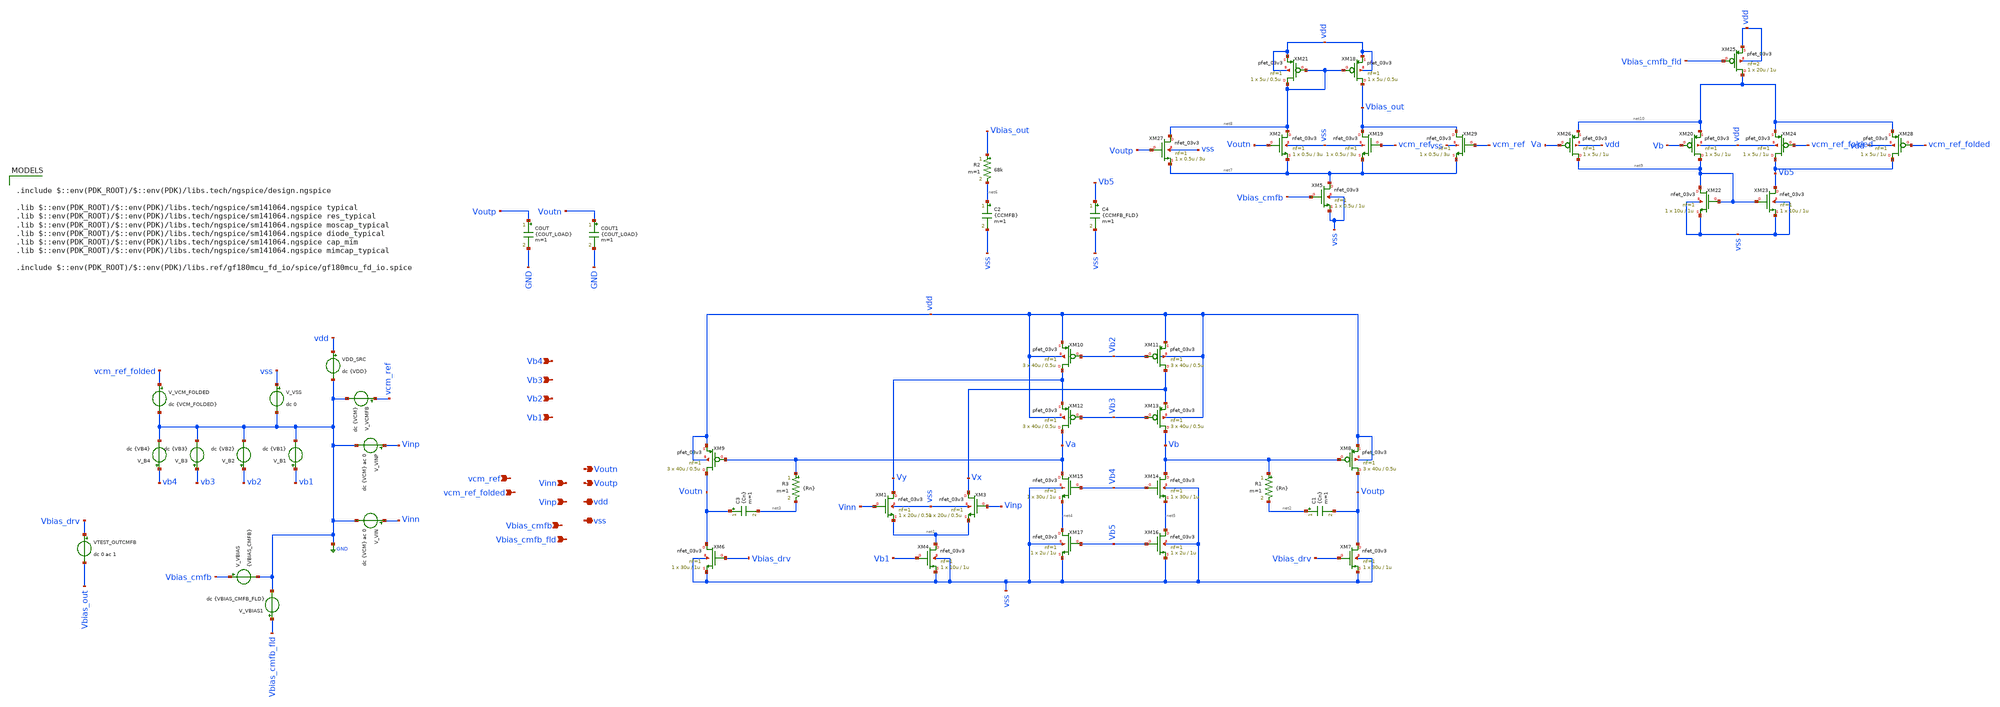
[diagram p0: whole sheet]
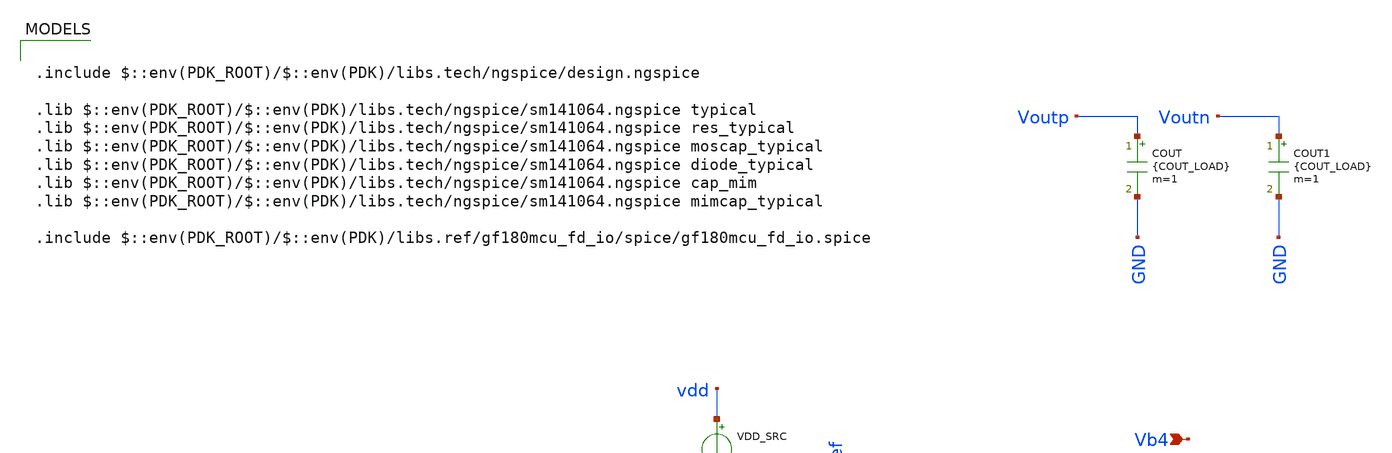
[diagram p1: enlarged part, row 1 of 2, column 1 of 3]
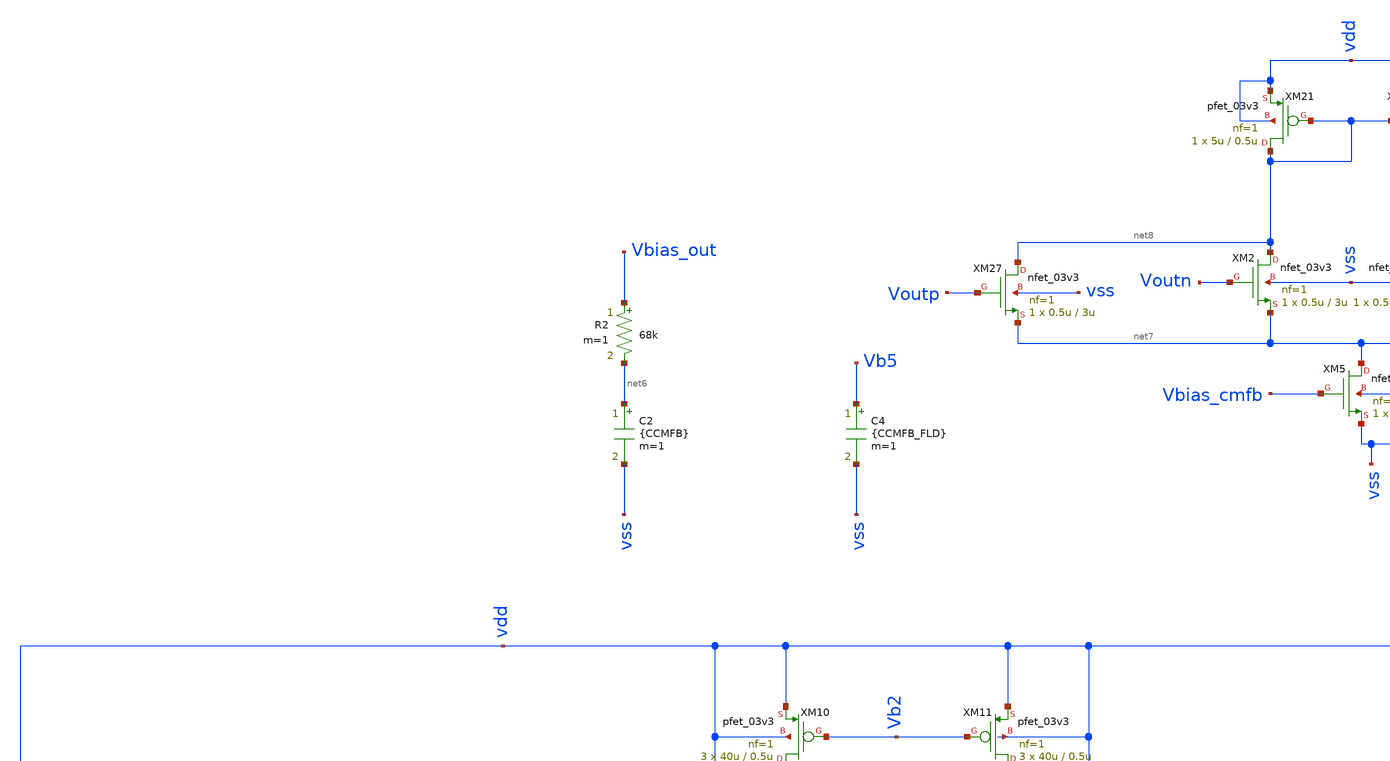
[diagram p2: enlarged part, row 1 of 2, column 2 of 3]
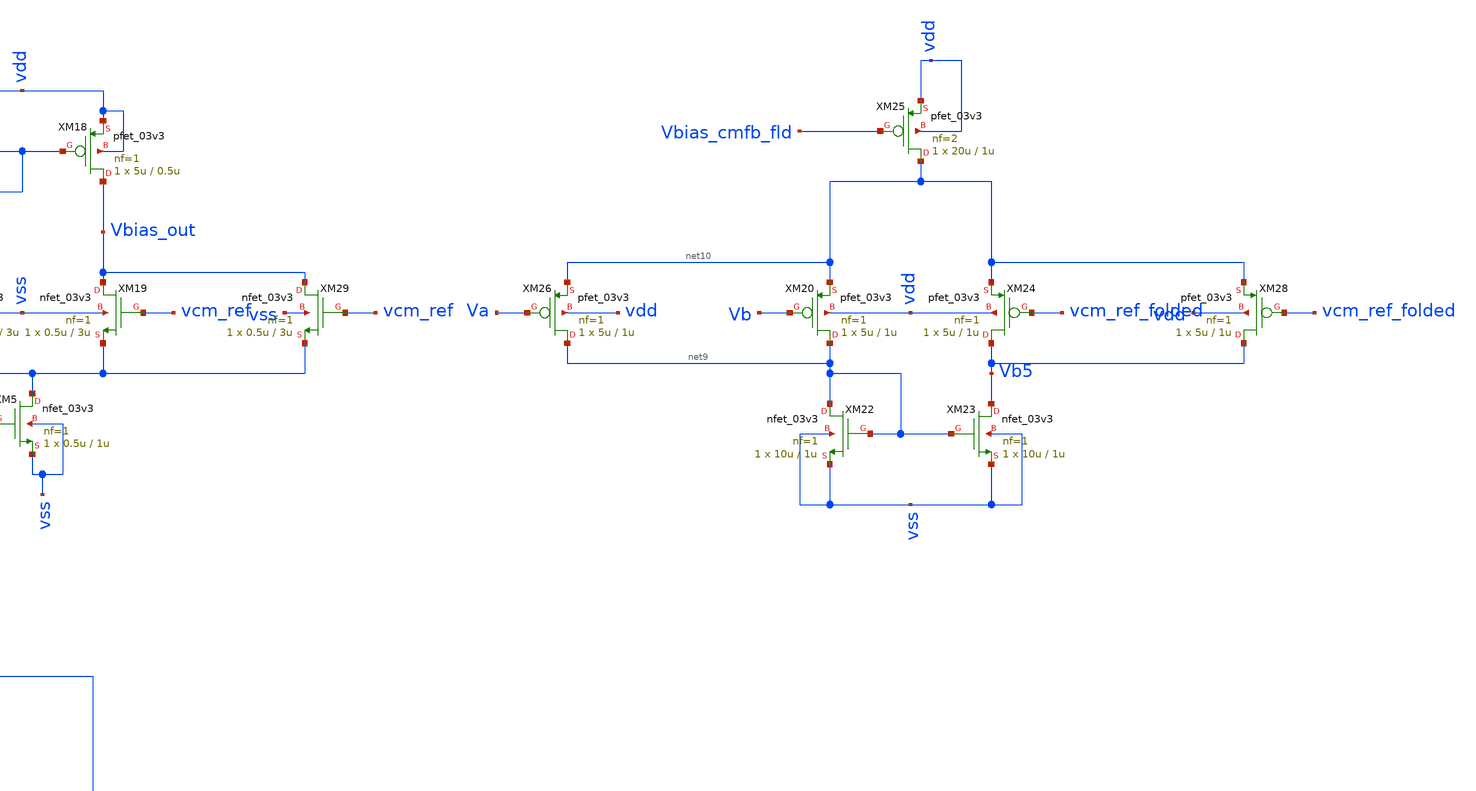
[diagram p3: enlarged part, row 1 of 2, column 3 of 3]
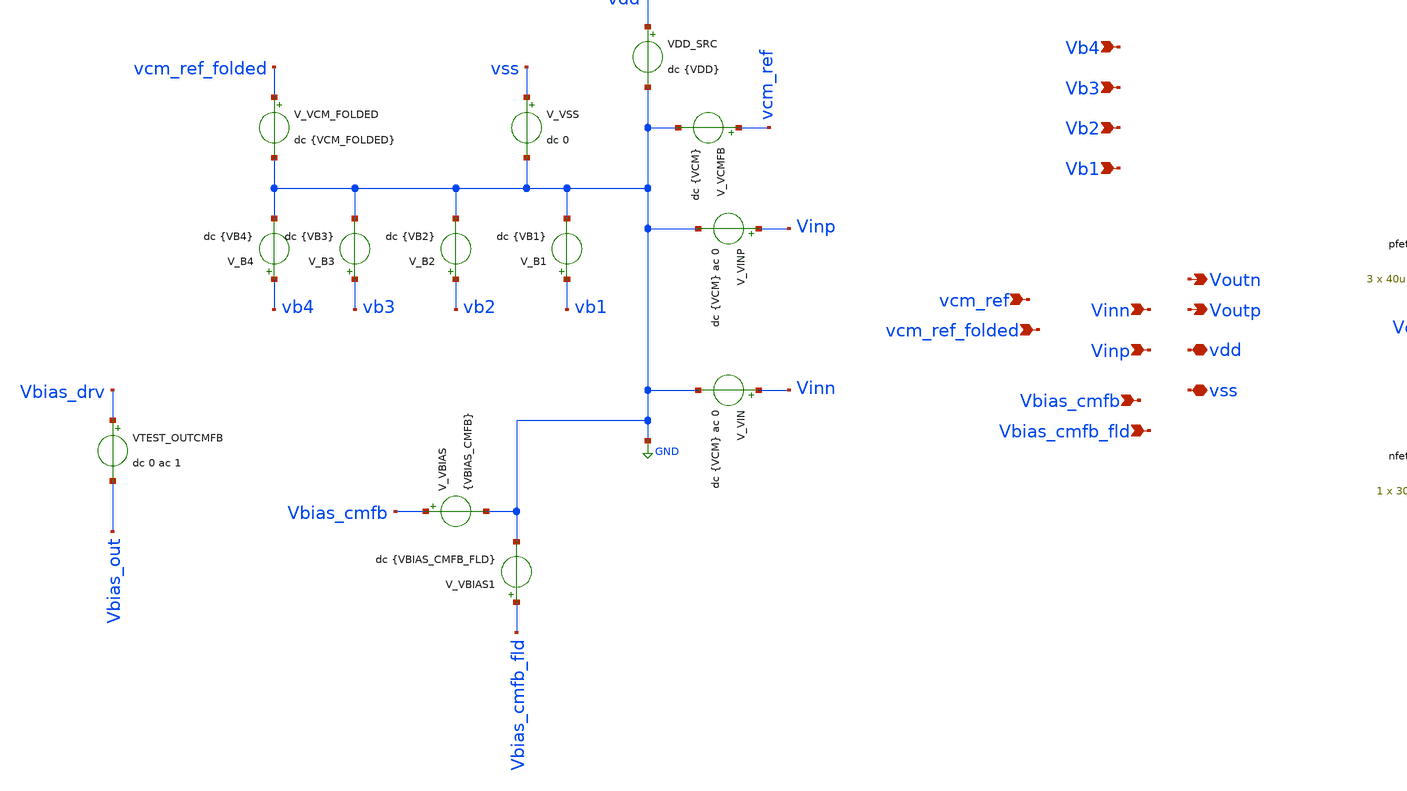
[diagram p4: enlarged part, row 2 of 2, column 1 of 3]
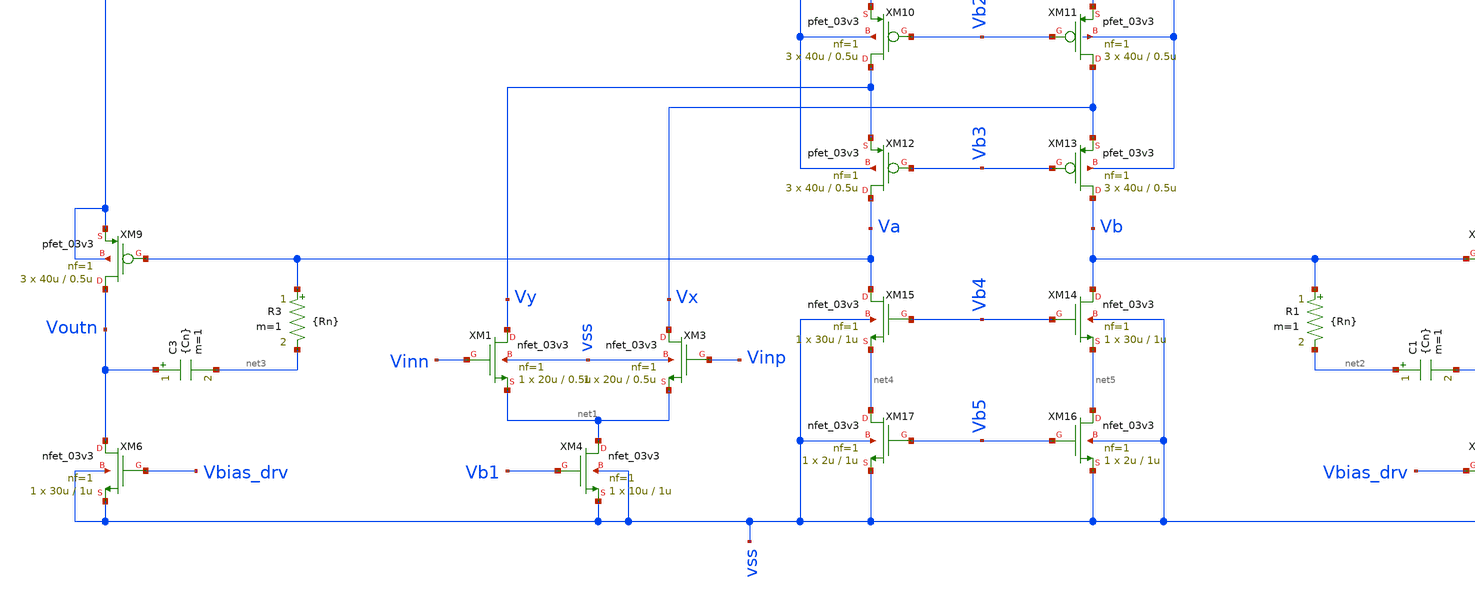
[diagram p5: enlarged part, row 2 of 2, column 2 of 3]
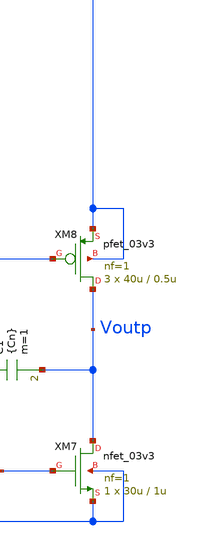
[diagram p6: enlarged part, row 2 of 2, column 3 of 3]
** sch_path: circuit_files/tb/op-amp_diff_looptest.sch
**.subckt op-amp_diff_looptest Vinn Voutp vdd Vinp Vb1 Vbias_cmfb_fld vss Voutn Vbias_cmfb Vb2 Vb3
*+ Vb4 vcm_ref_folded vcm_ref
*.ipin Vinn
*.opin Voutp
*.iopin vdd
*.ipin Vinp
*.ipin Vb1
*.ipin Vbias_cmfb_fld
*.iopin vss
*.opin Voutn
*.ipin Vbias_cmfb
*.ipin Vb2
*.ipin Vb3
*.ipin Vb4
*.ipin vcm_ref_folded
*.ipin vcm_ref
XM1 Vy Vinn net1 vss nfet_03v3 L=0.5u W=20u nf=1 ad='int((nf+1)/2) * W/nf * 0.18u' as='int((nf+2)/2) * W/nf * 0.18u'
+ pd='2*int((nf+1)/2) * (W/nf + 0.18u)' ps='2*int((nf+2)/2) * (W/nf + 0.18u)' nrd='0.18u / W' nrs='0.18u / W'
+ sa=0 sb=0 sd=0 m=1
XM4 net1 Vb1 vss vss nfet_03v3 L=1u W=10u nf=1 ad='int((nf+1)/2) * W/nf * 0.18u' as='int((nf+2)/2) * W/nf * 0.18u'
+ pd='2*int((nf+1)/2) * (W/nf + 0.18u)' ps='2*int((nf+2)/2) * (W/nf + 0.18u)' nrd='0.18u / W' nrs='0.18u / W'
+ sa=0 sb=0 sd=0 m=1
XM3 Vx Vinp net1 vss nfet_03v3 L=0.5u W=20u nf=1 ad='int((nf+1)/2) * W/nf * 0.18u' as='int((nf+2)/2) * W/nf * 0.18u'
+ pd='2*int((nf+1)/2) * (W/nf + 0.18u)' ps='2*int((nf+2)/2) * (W/nf + 0.18u)' nrd='0.18u / W' nrs='0.18u / W'
+ sa=0 sb=0 sd=0 m=1
XM7 Voutp Vbias_drv vss vss nfet_03v3 L=1u W=30u nf=1 ad='int((nf+1)/2) * W/nf * 0.18u' as='int((nf+2)/2) * W/nf * 0.18u'
+ pd='2*int((nf+1)/2) * (W/nf + 0.18u)' ps='2*int((nf+2)/2) * (W/nf + 0.18u)' nrd='0.18u / W' nrs='0.18u / W'
+ sa=0 sb=0 sd=0 m=1
XM8 Voutp Vb vdd vdd pfet_03v3 L=0.5u W=40u nf=1 ad='int((nf+1)/2) * W/nf * 0.18u' as='int((nf+2)/2) * W/nf * 0.18u'
+ pd='2*int((nf+1)/2) * (W/nf + 0.18u)' ps='2*int((nf+2)/2) * (W/nf + 0.18u)' nrd='0.18u / W' nrs='0.18u / W'
+ sa=0 sb=0 sd=0 m=3
XM6 Voutn Vbias_drv vss vss nfet_03v3 L=1u W=30u nf=1 ad='int((nf+1)/2) * W/nf * 0.18u' as='int((nf+2)/2) * W/nf * 0.18u'
+ pd='2*int((nf+1)/2) * (W/nf + 0.18u)' ps='2*int((nf+2)/2) * (W/nf + 0.18u)' nrd='0.18u / W' nrs='0.18u / W'
+ sa=0 sb=0 sd=0 m=1
XM9 Voutn Va vdd vdd pfet_03v3 L=0.5u W=40u nf=1 ad='int((nf+1)/2) * W/nf * 0.18u' as='int((nf+2)/2) * W/nf * 0.18u'
+ pd='2*int((nf+1)/2) * (W/nf + 0.18u)' ps='2*int((nf+2)/2) * (W/nf + 0.18u)' nrd='0.18u / W' nrs='0.18u / W'
+ sa=0 sb=0 sd=0 m=3
XM10 Vy Vb2 vdd vdd pfet_03v3 L=0.5u W=40u nf=1 ad='int((nf+1)/2) * W/nf * 0.18u' as='int((nf+2)/2) * W/nf * 0.18u'
+ pd='2*int((nf+1)/2) * (W/nf + 0.18u)' ps='2*int((nf+2)/2) * (W/nf + 0.18u)' nrd='0.18u / W' nrs='0.18u / W'
+ sa=0 sb=0 sd=0 m=3
XM11 Vx Vb2 vdd vdd pfet_03v3 L=0.5u W=40u nf=1 ad='int((nf+1)/2) * W/nf * 0.18u' as='int((nf+2)/2) * W/nf * 0.18u'
+ pd='2*int((nf+1)/2) * (W/nf + 0.18u)' ps='2*int((nf+2)/2) * (W/nf + 0.18u)' nrd='0.18u / W' nrs='0.18u / W'
+ sa=0 sb=0 sd=0 m=3
XM12 Va Vb3 Vy vdd pfet_03v3 L=0.5u W=40u nf=1 ad='int((nf+1)/2) * W/nf * 0.18u' as='int((nf+2)/2) * W/nf * 0.18u'
+ pd='2*int((nf+1)/2) * (W/nf + 0.18u)' ps='2*int((nf+2)/2) * (W/nf + 0.18u)' nrd='0.18u / W' nrs='0.18u / W'
+ sa=0 sb=0 sd=0 m=3
XM13 Vb Vb3 Vx vdd pfet_03v3 L=0.5u W=40u nf=1 ad='int((nf+1)/2) * W/nf * 0.18u' as='int((nf+2)/2) * W/nf * 0.18u'
+ pd='2*int((nf+1)/2) * (W/nf + 0.18u)' ps='2*int((nf+2)/2) * (W/nf + 0.18u)' nrd='0.18u / W' nrs='0.18u / W'
+ sa=0 sb=0 sd=0 m=3
XM14 Vb Vb4 net5 vss nfet_03v3 L=1u W=30u nf=1 ad='int((nf+1)/2) * W/nf * 0.18u' as='int((nf+2)/2) * W/nf * 0.18u'
+ pd='2*int((nf+1)/2) * (W/nf + 0.18u)' ps='2*int((nf+2)/2) * (W/nf + 0.18u)' nrd='0.18u / W' nrs='0.18u / W'
+ sa=0 sb=0 sd=0 m=1
XM15 Va Vb4 net4 vss nfet_03v3 L=1u W=30u nf=1 ad='int((nf+1)/2) * W/nf * 0.18u' as='int((nf+2)/2) * W/nf * 0.18u'
+ pd='2*int((nf+1)/2) * (W/nf + 0.18u)' ps='2*int((nf+2)/2) * (W/nf + 0.18u)' nrd='0.18u / W' nrs='0.18u / W'
+ sa=0 sb=0 sd=0 m=1
XM16 net5 Vb5 vss vss nfet_03v3 L=1u W=2u nf=1 ad='int((nf+1)/2) * W/nf * 0.18u' as='int((nf+2)/2) * W/nf * 0.18u'
+ pd='2*int((nf+1)/2) * (W/nf + 0.18u)' ps='2*int((nf+2)/2) * (W/nf + 0.18u)' nrd='0.18u / W' nrs='0.18u / W'
+ sa=0 sb=0 sd=0 m=1
XM17 net4 Vb5 vss vss nfet_03v3 L=1u W=2u nf=1 ad='int((nf+1)/2) * W/nf * 0.18u' as='int((nf+2)/2) * W/nf * 0.18u'
+ pd='2*int((nf+1)/2) * (W/nf + 0.18u)' ps='2*int((nf+2)/2) * (W/nf + 0.18u)' nrd='0.18u / W' nrs='0.18u / W'
+ sa=0 sb=0 sd=0 m=1
C3 Voutn net3 {Cn} m=1
R3 Va net3 {Rn} m=1
R1 Vb net2 {Rn} m=1
C1 net2 Voutp {Cn} m=1
C2 net6 vss {CCMFB} m=1
C4 Vb5 vss {CCMFB_FLD} m=1
V_VIN Vinn GND dc {VCM} ac 0
VDD_SRC vdd GND dc {VDD}
V_VINP Vinp GND dc {VCM} ac 0
V_VSS vss GND dc 0
V_VCMFB vcm_ref GND dc {VCM}
V_B1 vb1 GND dc {VB1}
V_B2 vb2 GND dc {VB2}
V_B3 vb3 GND dc {VB3}
V_B4 vb4 GND dc {VB4}
V_VCM_FOLDED vcm_ref_folded GND dc {VCM_FOLDED}
V_VBIAS Vbias_cmfb GND {VBIAS_CMFB}
V_VBIAS1 Vbias_cmfb_fld GND dc {VBIAS_CMFB_FLD}
COUT Voutp GND {COUT_LOAD} m=1
COUT1 Voutn GND {COUT_LOAD} m=1
VTEST_OUTCMFB Vbias_drv Vbias_out dc 0 ac 1
XM2 net8 Voutn net7 vss nfet_03v3 L=3u W=0.5u nf=1 ad='int((nf+1)/2) * W/nf * 0.18u' as='int((nf+2)/2) * W/nf * 0.18u'
+ pd='2*int((nf+1)/2) * (W/nf + 0.18u)' ps='2*int((nf+2)/2) * (W/nf + 0.18u)' nrd='0.18u / W' nrs='0.18u / W'
+ sa=0 sb=0 sd=0 m=1
XM5 net7 Vbias_cmfb vss vss nfet_03v3 L=1u W=0.5u nf=1 ad='int((nf+1)/2) * W/nf * 0.18u' as='int((nf+2)/2) * W/nf * 0.18u'
+ pd='2*int((nf+1)/2) * (W/nf + 0.18u)' ps='2*int((nf+2)/2) * (W/nf + 0.18u)' nrd='0.18u / W' nrs='0.18u / W'
+ sa=0 sb=0 sd=0 m=1
XM18 Vbias_out net8 vdd vdd pfet_03v3 L=0.5u W=5u nf=1 ad='int((nf+1)/2) * W/nf * 0.18u' as='int((nf+2)/2) * W/nf * 0.18u'
+ pd='2*int((nf+1)/2) * (W/nf + 0.18u)' ps='2*int((nf+2)/2) * (W/nf + 0.18u)' nrd='0.18u / W' nrs='0.18u / W'
+ sa=0 sb=0 sd=0 m=1
XM19 Vbias_out vcm_ref net7 vss nfet_03v3 L=3u W=0.5u nf=1 ad='int((nf+1)/2) * W/nf * 0.18u' as='int((nf+2)/2) * W/nf * 0.18u'
+ pd='2*int((nf+1)/2) * (W/nf + 0.18u)' ps='2*int((nf+2)/2) * (W/nf + 0.18u)' nrd='0.18u / W' nrs='0.18u / W'
+ sa=0 sb=0 sd=0 m=1
XM21 net8 net8 vdd vdd pfet_03v3 L=0.5u W=5u nf=1 ad='int((nf+1)/2) * W/nf * 0.18u' as='int((nf+2)/2) * W/nf * 0.18u'
+ pd='2*int((nf+1)/2) * (W/nf + 0.18u)' ps='2*int((nf+2)/2) * (W/nf + 0.18u)' nrd='0.18u / W' nrs='0.18u / W'
+ sa=0 sb=0 sd=0 m=1
XM20 net9 Vb net10 vdd pfet_03v3 L=1u W=5u nf=1 ad='int((nf+1)/2) * W/nf * 0.18u' as='int((nf+2)/2) * W/nf * 0.18u'
+ pd='2*int((nf+1)/2) * (W/nf + 0.18u)' ps='2*int((nf+2)/2) * (W/nf + 0.18u)' nrd='0.18u / W' nrs='0.18u / W'
+ sa=0 sb=0 sd=0 m=1
XM24 Vb5 vcm_ref_folded net10 vdd pfet_03v3 L=1u W=5u nf=1 ad='int((nf+1)/2) * W/nf * 0.18u' as='int((nf+2)/2) * W/nf * 0.18u'
+ pd='2*int((nf+1)/2) * (W/nf + 0.18u)' ps='2*int((nf+2)/2) * (W/nf + 0.18u)' nrd='0.18u / W' nrs='0.18u / W'
+ sa=0 sb=0 sd=0 m=1
XM22 net9 net9 vss vss nfet_03v3 L=1u W=10u nf=1 ad='int((nf+1)/2) * W/nf * 0.18u' as='int((nf+2)/2) * W/nf * 0.18u'
+ pd='2*int((nf+1)/2) * (W/nf + 0.18u)' ps='2*int((nf+2)/2) * (W/nf + 0.18u)' nrd='0.18u / W' nrs='0.18u / W'
+ sa=0 sb=0 sd=0 m=1
XM23 Vb5 net9 vss vss nfet_03v3 L=1u W=10u nf=1 ad='int((nf+1)/2) * W/nf * 0.18u' as='int((nf+2)/2) * W/nf * 0.18u'
+ pd='2*int((nf+1)/2) * (W/nf + 0.18u)' ps='2*int((nf+2)/2) * (W/nf + 0.18u)' nrd='0.18u / W' nrs='0.18u / W'
+ sa=0 sb=0 sd=0 m=1
XM25 net10 Vbias_cmfb_fld vdd vdd pfet_03v3 L=1u W=20u nf=2 ad='int((nf+1)/2) * W/nf * 0.18u' as='int((nf+2)/2) * W/nf * 0.18u'
+ pd='2*int((nf+1)/2) * (W/nf + 0.18u)' ps='2*int((nf+2)/2) * (W/nf + 0.18u)' nrd='0.18u / W' nrs='0.18u / W'
+ sa=0 sb=0 sd=0 m=1
XM26 net9 Va net10 vdd pfet_03v3 L=1u W=5u nf=1 ad='int((nf+1)/2) * W/nf * 0.18u' as='int((nf+2)/2) * W/nf * 0.18u'
+ pd='2*int((nf+1)/2) * (W/nf + 0.18u)' ps='2*int((nf+2)/2) * (W/nf + 0.18u)' nrd='0.18u / W' nrs='0.18u / W'
+ sa=0 sb=0 sd=0 m=1
XM28 Vb5 vcm_ref_folded net10 vdd pfet_03v3 L=1u W=5u nf=1 ad='int((nf+1)/2) * W/nf * 0.18u' as='int((nf+2)/2) * W/nf * 0.18u'
+ pd='2*int((nf+1)/2) * (W/nf + 0.18u)' ps='2*int((nf+2)/2) * (W/nf + 0.18u)' nrd='0.18u / W' nrs='0.18u / W'
+ sa=0 sb=0 sd=0 m=1
XM27 net8 Voutp net7 vss nfet_03v3 L=3u W=0.5u nf=1 ad='int((nf+1)/2) * W/nf * 0.18u' as='int((nf+2)/2) * W/nf * 0.18u'
+ pd='2*int((nf+1)/2) * (W/nf + 0.18u)' ps='2*int((nf+2)/2) * (W/nf + 0.18u)' nrd='0.18u / W' nrs='0.18u / W'
+ sa=0 sb=0 sd=0 m=1
XM29 Vbias_out vcm_ref net7 vss nfet_03v3 L=3u W=0.5u nf=1 ad='int((nf+1)/2) * W/nf * 0.18u' as='int((nf+2)/2) * W/nf * 0.18u'
+ pd='2*int((nf+1)/2) * (W/nf + 0.18u)' ps='2*int((nf+2)/2) * (W/nf + 0.18u)' nrd='0.18u / W' nrs='0.18u / W'
+ sa=0 sb=0 sd=0 m=1
R2 Vbias_out net6 68k m=1
**** begin user architecture code

.include $::env(PDK_ROOT)/$::env(PDK)/libs.tech/ngspice/design.ngspice

.lib $::env(PDK_ROOT)/$::env(PDK)/libs.tech/ngspice/sm141064.ngspice typical
.lib $::env(PDK_ROOT)/$::env(PDK)/libs.tech/ngspice/sm141064.ngspice res_typical
.lib $::env(PDK_ROOT)/$::env(PDK)/libs.tech/ngspice/sm141064.ngspice moscap_typical
.lib $::env(PDK_ROOT)/$::env(PDK)/libs.tech/ngspice/sm141064.ngspice diode_typical
.lib $::env(PDK_ROOT)/$::env(PDK)/libs.tech/ngspice/sm141064.ngspice cap_mim
.lib $::env(PDK_ROOT)/$::env(PDK)/libs.tech/ngspice/sm141064.ngspice mimcap_typical

.include $::env(PDK_ROOT)/$::env(PDK)/libs.ref/gf180mcu_fd_io/spice/gf180mcu_fd_io.spice



.param VDD=3.3
.param VCM=1.65
.param VCM_FOLDED=2.40

.param VB1=0.58
.param VB2=2.637
.param VB3=2.25
.param VB4=1.15

.param VBIAS_CMFB=0.82
.param VBIAS_CMFB_FLD=2.55

.param Cn=500f
.param Rn=8k
.param COUT_LOAD=200f

.param CCMFB=50p
.param CCMFB_FLD=1p

.options reltol=1e-4 abstol=1e-12 vntol=1e-6
.options gmin=1e-12
.options plotwinsize=0
.options method=gear maxord=2

.nodeset V(voutp)=1.641
.nodeset V(voutn)=1.641
.nodeset V(vbias_out)=0.866
.nodeset V(vbias_drv)=0.866
.nodeset V(va)=2.401
.nodeset V(vb)=2.401
.nodeset V(vb5)=0.716
.nodeset V(net8)=0.576
.nodeset V(net9)=3.194

.control

set noaskquit
set measdgt=8
save all

shell rm -f outcmfb_loop_report.txt
shell rm -f outcmfb_loop_response.txt

echo ================================================== > outcmfb_loop_report.txt
echo OUTPUT CMFB LOOP TEST >> outcmfb_loop_report.txt
echo ================================================== >> outcmfb_loop_report.txt

op

let voutcm_op     = 0.5*(v(voutp)+v(voutn))
let out_cm_err    = voutcm_op-1.65
let va_cm_op      = 0.5*(v(va)+v(vb))
let folded_cm_err = va_cm_op - v(vcm_ref_folded)
let idd_op        = -i(VDD_SRC)
let pdc_op        = 3.3*idd_op

echo ---------------- OP CHECK ---------------- >> outcmfb_loop_report.txt
echo VOUTP=$&v(voutp) >> outcmfb_loop_report.txt
echo VOUTN=$&v(voutn) >> outcmfb_loop_report.txt
echo VOUTCM=$&voutcm_op >> outcmfb_loop_report.txt
echo OUT_CM_ERR=$&out_cm_err >> outcmfb_loop_report.txt

echo VBIAS_OUT=$&v(vbias_out) >> outcmfb_loop_report.txt
echo VBIAS_DRV=$&v(vbias_drv) >> outcmfb_loop_report.txt
echo VA=$&v(va) >> outcmfb_loop_report.txt
echo VB=$&v(vb) >> outcmfb_loop_report.txt
echo VA_CM=$&va_cm_op >> outcmfb_loop_report.txt

echo FOLDED_CM_ERR=$&folded_cm_err >> outcmfb_loop_report.txt
echo IDD=$&idd_op >> outcmfb_loop_report.txt
echo PDC=$&pdc_op >> outcmfb_loop_report.txt
echo -------------------------------------------------- >> outcmfb_loop_report.txt

ac dec 200 1 1G

let outcmfb_inj          = v(vbias_drv)-v(vbias_out)

let outcmfb_return_ratio = -v(vbias_out)/(outcmfb_inj+1e-30)

let outcmfb_loop         = outcmfb_return_ratio/(1-outcmfb_return_ratio+1e-30)
let outcmfb_loop_db      = 20*log10(mag(outcmfb_loop)+1e-30)

let outcmfb_phase_rad    = cph(outcmfb_loop)
let outcmfb_phase_deg    = 57.2957795*outcmfb_phase_rad

meas ac OUTCMFB_GAIN_1HZ_DB  find outcmfb_loop_db at=1
meas ac OUTCMFB_PHASE_1HZ    find outcmfb_phase_deg at=1
meas ac OUTCMFB_UGF          when outcmfb_loop_db=0 fall=1
meas ac OUTCMFB_PHASE_UGF    find outcmfb_phase_deg when outcmfb_loop_db=0 fall=1

let outcmfb_phase_ugf_wrapped = outcmfb_phase_ugf

while outcmfb_phase_ugf_wrapped < -180
  let outcmfb_phase_ugf_wrapped = outcmfb_phase_ugf_wrapped + 360
end

while outcmfb_phase_ugf_wrapped > 180
  let outcmfb_phase_ugf_wrapped = outcmfb_phase_ugf_wrapped - 360
end

let OUTCMFB_PM_RAW = 180 + outcmfb_phase_ugf
let OUTCMFB_PM_WRAPPED = 180 + outcmfb_phase_ugf_wrapped

meas ac OUTCMFB_GAIN_10K     find outcmfb_loop_db at=10k
meas ac OUTCMFB_GAIN_100K    find outcmfb_loop_db at=100k
meas ac OUTCMFB_GAIN_1MEG    find outcmfb_loop_db at=1Meg
meas ac OUTCMFB_PHASE_10K    find outcmfb_phase_deg at=10k
meas ac OUTCMFB_PHASE_100K   find outcmfb_phase_deg at=100k
meas ac OUTCMFB_PHASE_1MEG   find outcmfb_phase_deg at=1Meg

echo ---------------- OUTPUT CMFB LOOP RESULTS ---------------- >> outcmfb_loop_report.txt
echo LOOP_GAIN_1HZ_DB=$&outcmfb_gain_1hz_db >> outcmfb_loop_report.txt
echo PHASE_1HZ_DEG=$&outcmfb_phase_1hz >> outcmfb_loop_report.txt
echo UGF_HZ=$&outcmfb_ugf >> outcmfb_loop_report.txt
echo PHASE_AT_UGF_DEG=$&outcmfb_phase_ugf >> outcmfb_loop_report.txt
echo PHASE_MARGIN_DEG=$&OUTCMFB_PM >> outcmfb_loop_report.txt
echo GAIN_10K_DB=$&outcmfb_gain_10k PHASE_10K_DEG=$&outcmfb_phase_10k >> outcmfb_loop_report.txt
echo GAIN_100K_DB=$&outcmfb_gain_100k PHASE_100K_DEG=$&outcmfb_phase_100k >> outcmfb_loop_report.txt
echo GAIN_1MEG_DB=$&outcmfb_gain_1meg PHASE_1MEG_DEG=$&outcmfb_phase_1meg >> outcmfb_loop_report.txt
echo PHASE_AT_UGF_RAW_DEG=$&outcmfb_phase_ugf >> outcmfb_loop_report.txt
echo PHASE_AT_UGF_WRAPPED_DEG=$&outcmfb_phase_ugf_wrapped >> outcmfb_loop_report.txt
echo PHASE_MARGIN_RAW_DEG=$&OUTCMFB_PM_RAW >> outcmfb_loop_report.txt
echo PHASE_AT_UGF_WRAPPED_DEG=$&outcmfb_phase_ugf_wrapped >> outcmfb_loop_report.txt
echo PHASE_MARGIN_WRAPPED_DEG=$&OUTCMFB_PM_WRAPPED >> outcmfb_loop_report.txt
echo PHASE_MARGIN_DEG=$&OUTCMFB_PM >> outcmfb_loop_report.txt
echo -------------------------------------------------- >> outcmfb_loop_report.txt

wrdata outcmfb_loop_response.txt outcmfb_loop_db outcmfb_phase_deg outcmfb_return_ratio

print outcmfb_gain_1hz_db outcmfb_phase_1hz
print outcmfb_ugf outcmfb_phase_ugf OUTCMFB_PM

echo Done output CMFB loop test.

.endc


**** end user architecture code
**.ends
.GLOBAL GND
.end
